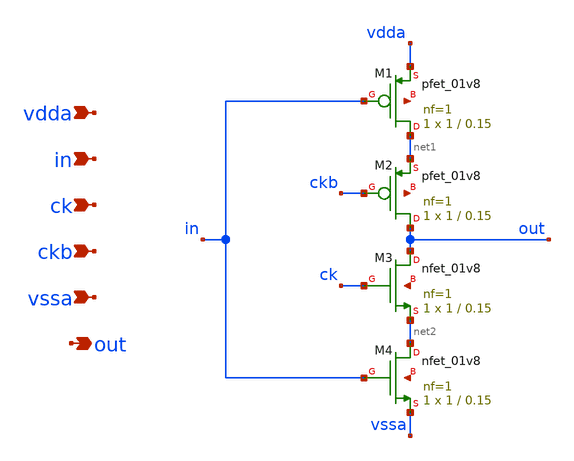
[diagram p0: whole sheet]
** sch_path: xschem/schematics/dac_sw.sch
**.subckt dac_sw vdda in ck ckb vssa out
*.ipin vdda
*.ipin in
*.ipin ck
*.ipin ckb
*.ipin vssa
*.opin out
XM1 net1 in vdda net3 sky130_fd_pr__pfet_01v8 L=0.15 W=1 nf=1 ad='int((nf+1)/2) * W/nf * 0.29' as='int((nf+2)/2) * W/nf * 0.29'
+ pd='2*int((nf+1)/2) * (W/nf + 0.29)' ps='2*int((nf+2)/2) * (W/nf + 0.29)' nrd='0.29 / W' nrs='0.29 / W'
+ sa=0 sb=0 sd=0 mult=1 m=1
XM2 out ckb net1 net4 sky130_fd_pr__pfet_01v8 L=0.15 W=1 nf=1 ad='int((nf+1)/2) * W/nf * 0.29' as='int((nf+2)/2) * W/nf * 0.29'
+ pd='2*int((nf+1)/2) * (W/nf + 0.29)' ps='2*int((nf+2)/2) * (W/nf + 0.29)' nrd='0.29 / W' nrs='0.29 / W'
+ sa=0 sb=0 sd=0 mult=1 m=1
XM3 out ck net2 net5 sky130_fd_pr__nfet_01v8 L=0.15 W=1 nf=1 ad='int((nf+1)/2) * W/nf * 0.29' as='int((nf+2)/2) * W/nf * 0.29'
+ pd='2*int((nf+1)/2) * (W/nf + 0.29)' ps='2*int((nf+2)/2) * (W/nf + 0.29)' nrd='0.29 / W' nrs='0.29 / W'
+ sa=0 sb=0 sd=0 mult=1 m=1
XM4 net2 in vssa net6 sky130_fd_pr__nfet_01v8 L=0.15 W=1 nf=1 ad='int((nf+1)/2) * W/nf * 0.29' as='int((nf+2)/2) * W/nf * 0.29'
+ pd='2*int((nf+1)/2) * (W/nf + 0.29)' ps='2*int((nf+2)/2) * (W/nf + 0.29)' nrd='0.29 / W' nrs='0.29 / W'
+ sa=0 sb=0 sd=0 mult=1 m=1
**.ends
.end
